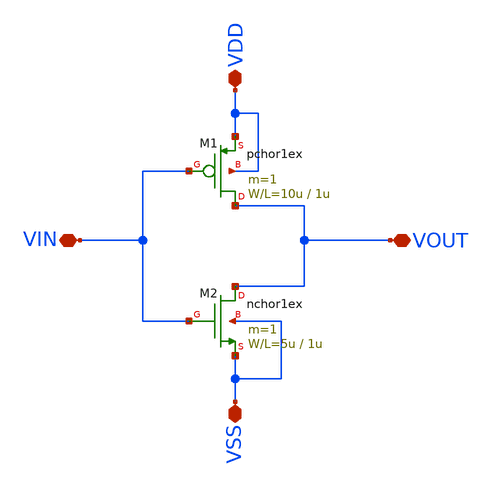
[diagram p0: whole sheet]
** sch_path: member_project/f0r3st/inverter.sch
**.subckt inverter VOUT VIN VDD VSS
*.iopin VOUT
*.iopin VIN
*.iopin VDD
*.iopin VSS
M1 VOUT VIN VDD VDD pchor1ex L=1u W=10u m=1
M2 VOUT VIN VSS VSS nchor1ex L=1u W=5u m=1
**.ends
.end
